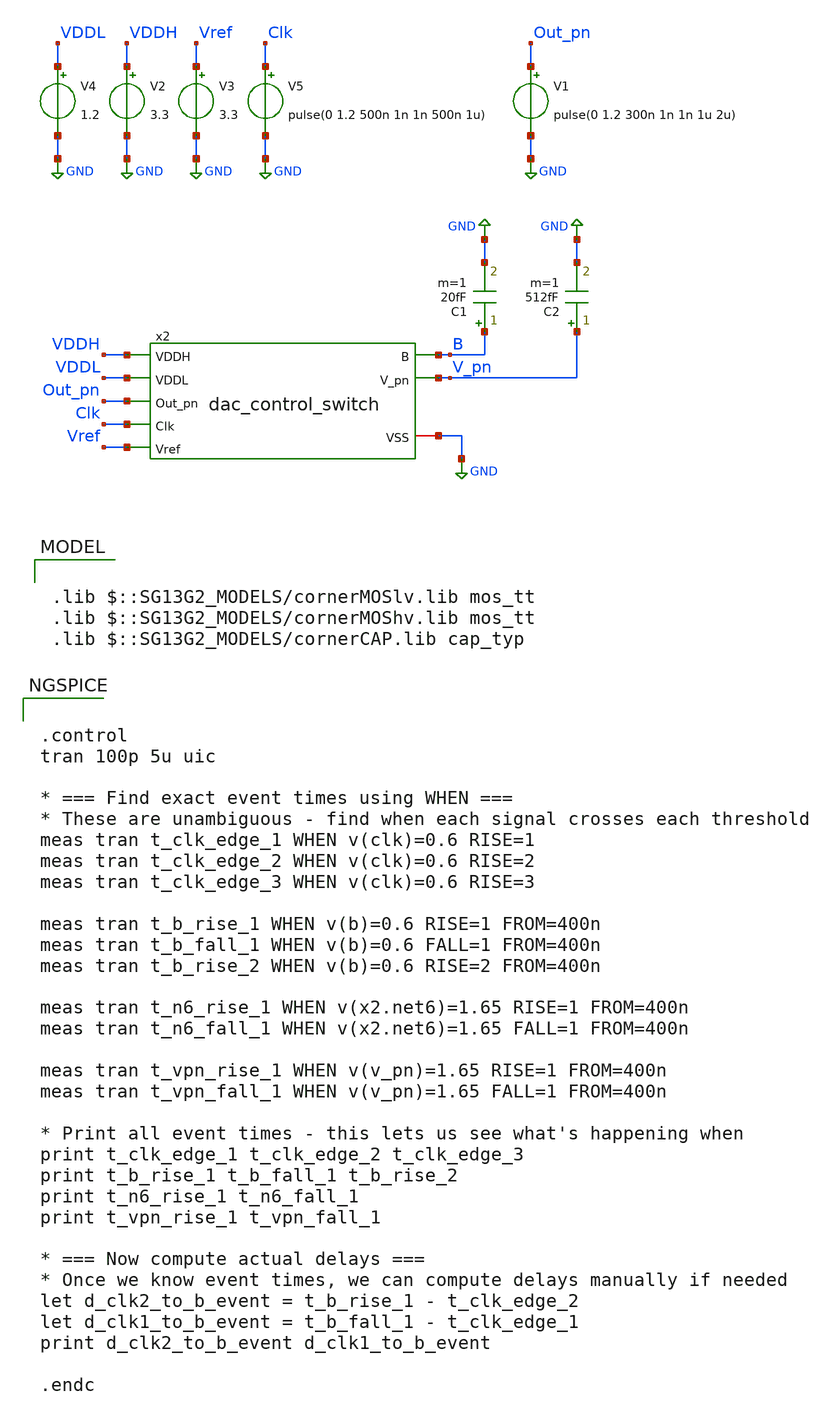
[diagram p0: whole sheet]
** sch_path: sar_adc/xschem/blocks/switch/dac_control_switch_tb.sch
**.subckt dac_control_switch_tb
V3 Vref GND 3.3
V4 VDDL GND 1.2
V5 Clk GND pulse(0 1.2 500n 1n 1n 500n 1u)
V1 Out_pn GND pulse(0 1.2 300n 1n 1n 1u 2u)
x2 VDDL VDDH Out_pn B Clk Vref V_pn GND dac_control_switch
V2 VDDH GND 3.3
C1 B GND 20fF m=1
C2 V_pn GND 512fF m=1
**** begin user architecture code

.lib $::SG13G2_MODELS/cornerMOSlv.lib mos_tt
.lib $::SG13G2_MODELS/cornerMOShv.lib mos_tt
.lib $::SG13G2_MODELS/cornerCAP.lib cap_typ



.control
tran 100p 5u uic

* === Find exact event times using WHEN ===
* These are unambiguous - find when each signal crosses each threshold
meas tran t_clk_edge_1 WHEN v(clk)=0.6 RISE=1
meas tran t_clk_edge_2 WHEN v(clk)=0.6 RISE=2
meas tran t_clk_edge_3 WHEN v(clk)=0.6 RISE=3

meas tran t_b_rise_1 WHEN v(b)=0.6 RISE=1 FROM=400n
meas tran t_b_fall_1 WHEN v(b)=0.6 FALL=1 FROM=400n
meas tran t_b_rise_2 WHEN v(b)=0.6 RISE=2 FROM=400n

meas tran t_n6_rise_1 WHEN v(x2.net6)=1.65 RISE=1 FROM=400n
meas tran t_n6_fall_1 WHEN v(x2.net6)=1.65 FALL=1 FROM=400n

meas tran t_vpn_rise_1 WHEN v(v_pn)=1.65 RISE=1 FROM=400n
meas tran t_vpn_fall_1 WHEN v(v_pn)=1.65 FALL=1 FROM=400n

* Print all event times - this lets us see what's happening when
print t_clk_edge_1 t_clk_edge_2 t_clk_edge_3
print t_b_rise_1 t_b_fall_1 t_b_rise_2
print t_n6_rise_1 t_n6_fall_1
print t_vpn_rise_1 t_vpn_fall_1

* === Now compute actual delays ===
* Once we know event times, we can compute delays manually if needed
let d_clk2_to_b_event = t_b_rise_1 - t_clk_edge_2
let d_clk1_to_b_event = t_b_fall_1 - t_clk_edge_1
print d_clk2_to_b_event d_clk1_to_b_event

.endc


**** end user architecture code
**.ends
.GLOBAL GND
.end
